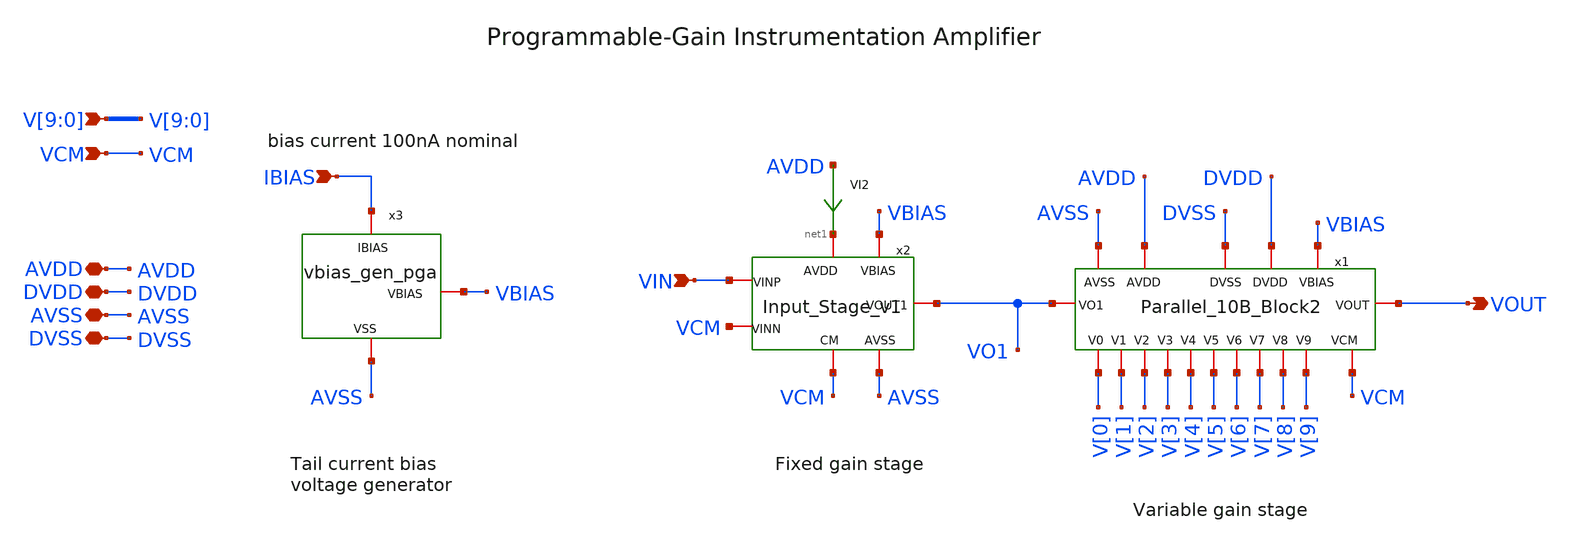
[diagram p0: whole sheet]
** sch_path: xschem/sky130_pa_ip__opamp.sch
**.subckt sky130_pa_ip__opamp VCM AVDD VOUT IBIAS DVDD AVSS DVSS
*+ V[9],V[8],V[7],V[6],V[5],V[4],V[3],V[2],V[1],V[0] VIN
*.ipin VCM
*.iopin AVDD
*.opin VOUT
*.ipin IBIAS
*.iopin DVDD
*.iopin AVSS
*.iopin DVSS
*.ipin V[9],V[8],V[7],V[6],V[5],V[4],V[3],V[2],V[1],V[0]
*.ipin VIN
x1 V[6] V[5] V[8] V[9] V[7] VO1 DVDD AVDD VOUT V[4] V[3] V[2] V[1] V[0] VCM DVSS AVSS VBIAS
+ Parallel_10B_Block2
x2 net1 VIN VO1 VCM VCM AVSS VBIAS Input_Stage_v1
VI2 AVDD net1 0
.save i(vi2)
x3 VBIAS IBIAS AVSS vbias_gen_pga
**.ends
.end
